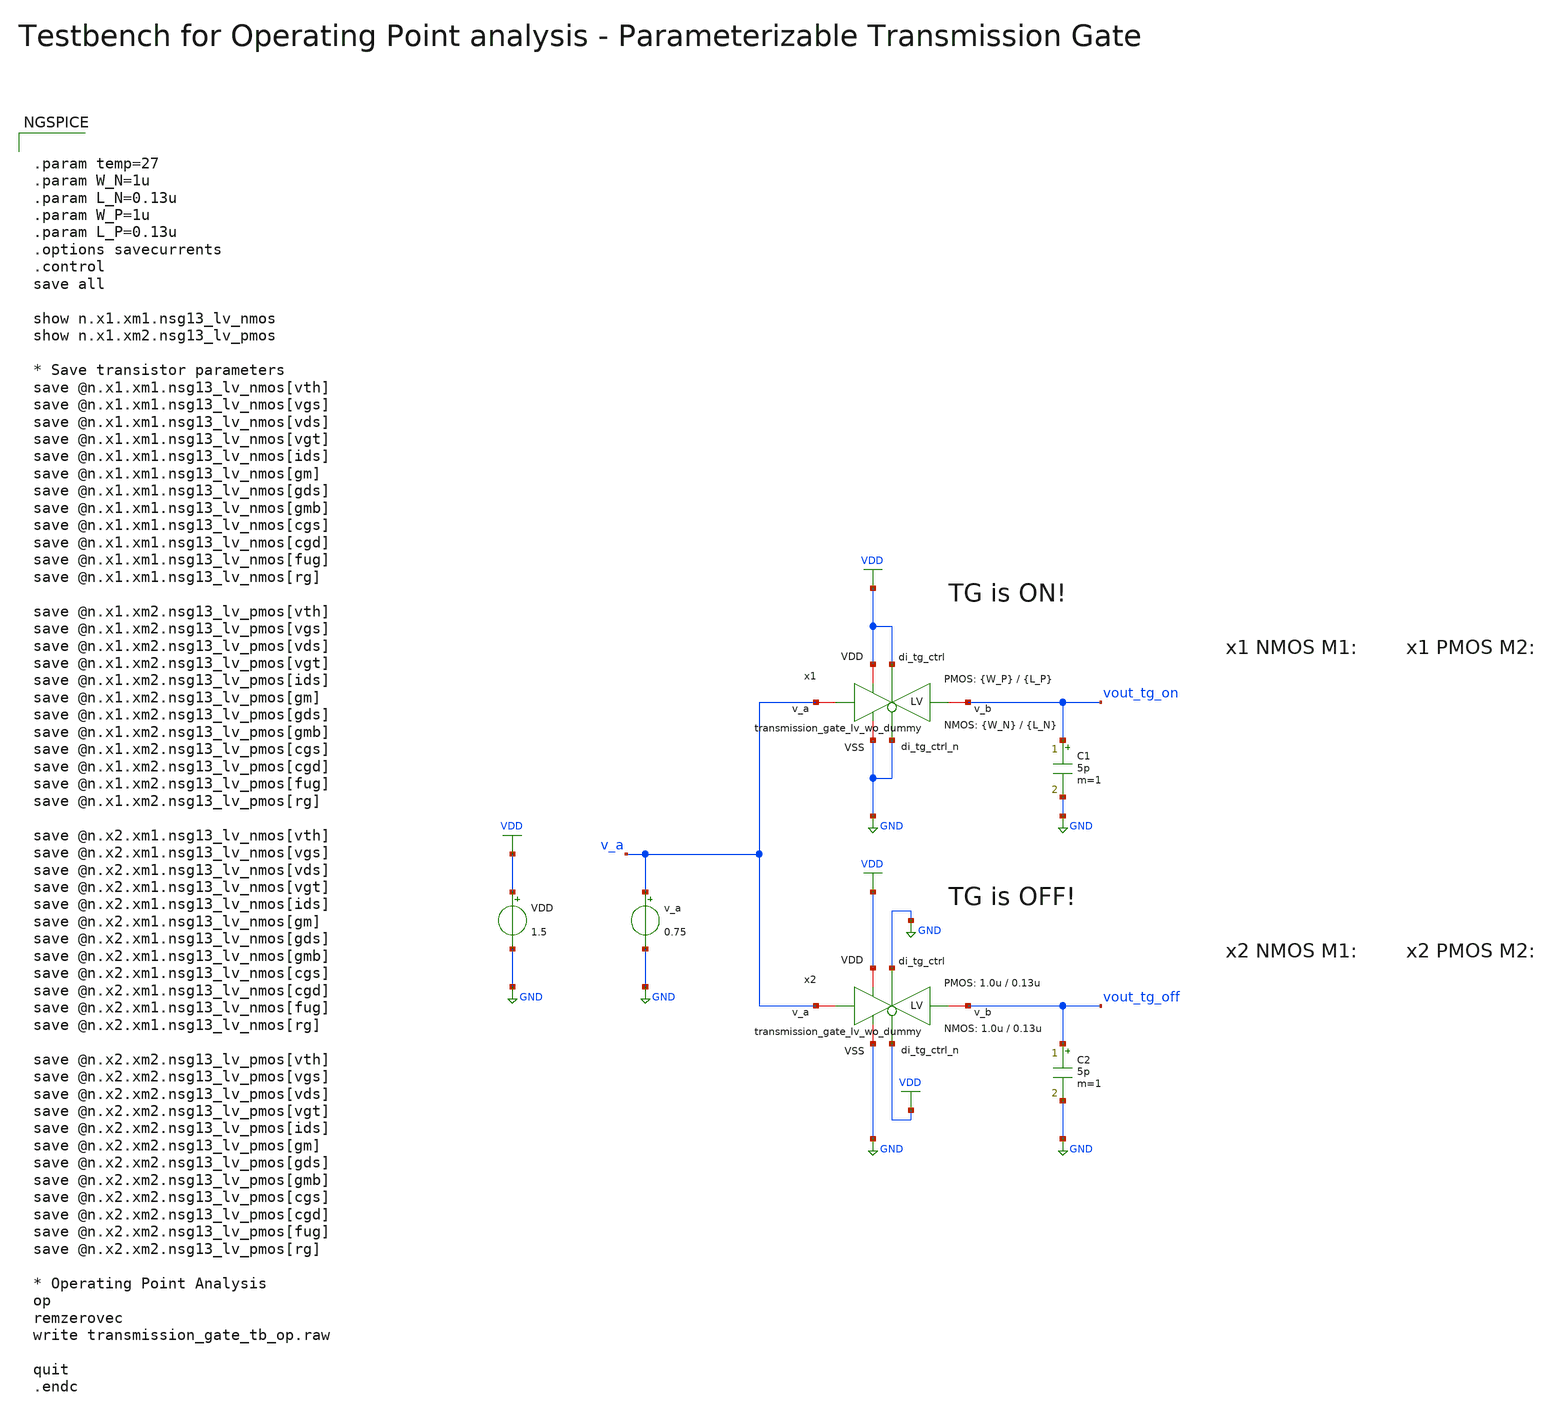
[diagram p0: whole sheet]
** sch_path: SG13G2_ATBS-ADC-main/xschem/transmission_gate/testbenches/transmission_gate_tb_op.sch
**.subckt transmission_gate_tb_op
v_a v_a GND 0.75
VDD VDD GND 1.5
C1 vout_tg_on GND 5p m=1
C2 vout_tg_off GND 5p m=1
x1 VDD VDD GND vout_tg_on v_a GND transmission_gate_lv_wo_dummy W_P={W_P} L_P={L_P} W_N={W_N} L_N={L_N}
x2 VDD GND GND vout_tg_off v_a VDD transmission_gate_lv_wo_dummy W_P=1.0u L_P=0.13u W_N=1.0u
+ L_N=0.13u
**** begin user architecture code

.lib cornerMOShv.lib mos_tt
.lib cornerMOSlv.lib mos_tt
.lib cornerRES.lib res_typ



.param temp=27
.param W_N=1u
.param L_N=0.13u
.param W_P=1u
.param L_P=0.13u
.options savecurrents
.control
save all

show n.x1.xm1.nsg13_lv_nmos
show n.x1.xm2.nsg13_lv_pmos

* Save transistor parameters
save @n.x1.xm1.nsg13_lv_nmos[vth]
save @n.x1.xm1.nsg13_lv_nmos[vgs]
save @n.x1.xm1.nsg13_lv_nmos[vds]
save @n.x1.xm1.nsg13_lv_nmos[vgt]
save @n.x1.xm1.nsg13_lv_nmos[ids]
save @n.x1.xm1.nsg13_lv_nmos[gm]
save @n.x1.xm1.nsg13_lv_nmos[gds]
save @n.x1.xm1.nsg13_lv_nmos[gmb]
save @n.x1.xm1.nsg13_lv_nmos[cgs]
save @n.x1.xm1.nsg13_lv_nmos[cgd]
save @n.x1.xm1.nsg13_lv_nmos[fug]
save @n.x1.xm1.nsg13_lv_nmos[rg]

save @n.x1.xm2.nsg13_lv_pmos[vth]
save @n.x1.xm2.nsg13_lv_pmos[vgs]
save @n.x1.xm2.nsg13_lv_pmos[vds]
save @n.x1.xm2.nsg13_lv_pmos[vgt]
save @n.x1.xm2.nsg13_lv_pmos[ids]
save @n.x1.xm2.nsg13_lv_pmos[gm]
save @n.x1.xm2.nsg13_lv_pmos[gds]
save @n.x1.xm2.nsg13_lv_pmos[gmb]
save @n.x1.xm2.nsg13_lv_pmos[cgs]
save @n.x1.xm2.nsg13_lv_pmos[cgd]
save @n.x1.xm2.nsg13_lv_pmos[fug]
save @n.x1.xm2.nsg13_lv_pmos[rg]

save @n.x2.xm1.nsg13_lv_nmos[vth]
save @n.x2.xm1.nsg13_lv_nmos[vgs]
save @n.x2.xm1.nsg13_lv_nmos[vds]
save @n.x2.xm1.nsg13_lv_nmos[vgt]
save @n.x2.xm1.nsg13_lv_nmos[ids]
save @n.x2.xm1.nsg13_lv_nmos[gm]
save @n.x2.xm1.nsg13_lv_nmos[gds]
save @n.x2.xm1.nsg13_lv_nmos[gmb]
save @n.x2.xm1.nsg13_lv_nmos[cgs]
save @n.x2.xm1.nsg13_lv_nmos[cgd]
save @n.x2.xm1.nsg13_lv_nmos[fug]
save @n.x2.xm1.nsg13_lv_nmos[rg]

save @n.x2.xm2.nsg13_lv_pmos[vth]
save @n.x2.xm2.nsg13_lv_pmos[vgs]
save @n.x2.xm2.nsg13_lv_pmos[vds]
save @n.x2.xm2.nsg13_lv_pmos[vgt]
save @n.x2.xm2.nsg13_lv_pmos[ids]
save @n.x2.xm2.nsg13_lv_pmos[gm]
save @n.x2.xm2.nsg13_lv_pmos[gds]
save @n.x2.xm2.nsg13_lv_pmos[gmb]
save @n.x2.xm2.nsg13_lv_pmos[cgs]
save @n.x2.xm2.nsg13_lv_pmos[cgd]
save @n.x2.xm2.nsg13_lv_pmos[fug]
save @n.x2.xm2.nsg13_lv_pmos[rg]

* Operating Point Analysis
op
remzerovec
write transmission_gate_tb_op.raw

quit
.endc

**** end user architecture code
**.ends

* expanding   symbol:  transmission_gate/transmission_gate_lv_wo_dummy.sym # of pins=6
** sym_path: SG13G2_ATBS-ADC-main/xschem/transmission_gate/transmission_gate_lv_wo_dummy.sym
** sch_path: SG13G2_ATBS-ADC-main/xschem/transmission_gate/transmission_gate_lv_wo_dummy.sch
.subckt transmission_gate_lv_wo_dummy VDD di_tg_ctrl VSS v_b v_a di_tg_ctrl_n  W_P=1.0u L_P=0.13u
+ W_N=1.0u L_N=0.13u
*.iopin v_a
*.iopin v_b
*.iopin VDD
*.iopin VSS
*.ipin di_tg_ctrl
*.ipin di_tg_ctrl_n
XM1 v_a di_tg_ctrl v_b VSS sg13_lv_nmos w=W_N l=L_N ng=1 m=1 mm_ok=1
XM2 v_a di_tg_ctrl_n v_b VDD sg13_lv_pmos w=W_P l=L_P ng=1 m=1 mm_ok=1
.ends

.GLOBAL GND
.GLOBAL VDD
.end
